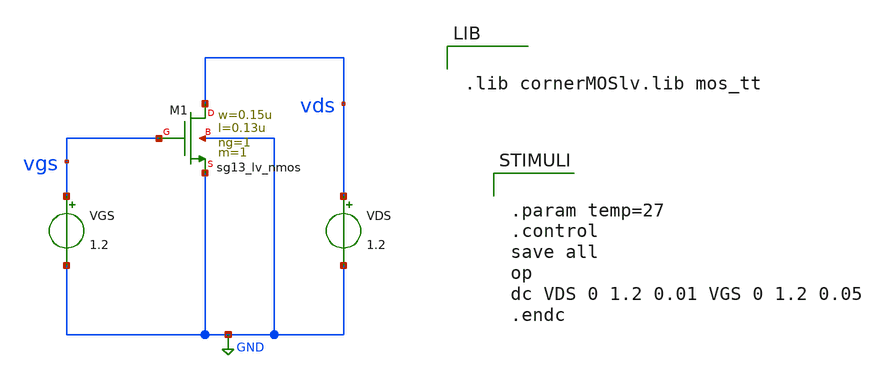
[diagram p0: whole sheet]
** sch_path: BTDay1-Ex/Ex2_Lecture1.sch
**.subckt Ex2_Lecture1
XM1 vds vgs GND GND sg13_lv_nmos w=0.15u l=0.13u ng=1 m=1 mm_ok=1
VGS vgs GND 1.2
VDS vds GND 1.2
**** begin user architecture code


.lib cornerMOSlv.lib mos_tt




.param temp=27
.control
save all
op
dc VDS 0 1.2 0.01 VGS 0 1.2 0.05
.endc


**** end user architecture code
**.ends
.GLOBAL GND
.end
